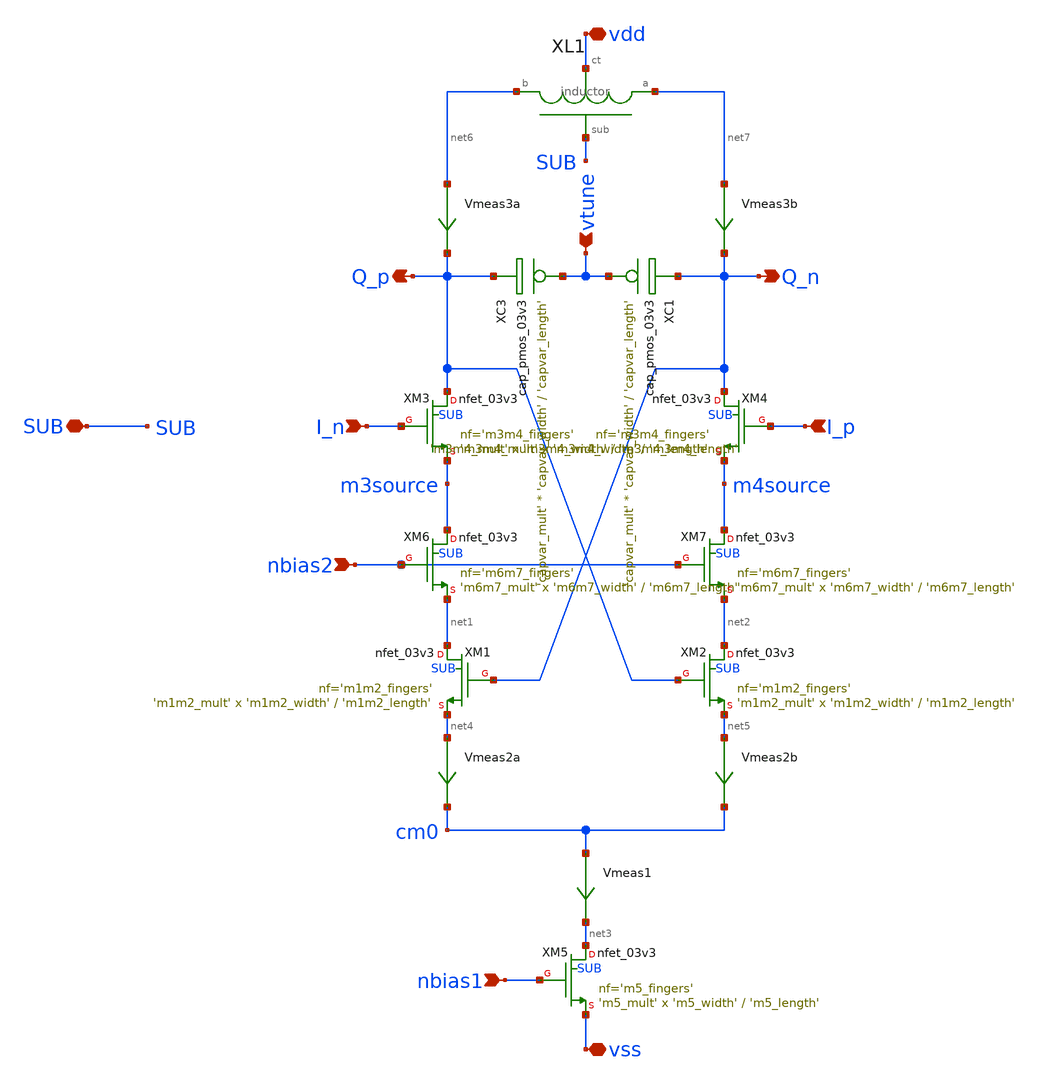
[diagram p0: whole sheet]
** sch_path: sch/vco/half_qvco_cascode_pair.sch
**.subckt half_qvco_cascode_pair SUB vdd vss I_n nbias1 Q_p Q_n I_p vtune nbias2
*.iopin SUB
*.iopin vdd
*.iopin vss
*.ipin I_n
*.ipin nbias1
*.opin Q_p
*.opin Q_n
*.ipin I_p
*.ipin vtune
*.ipin nbias2
XL1 vdd net7 SUB net6 inductor
XM5 net3 nbias1 vss SUB nfet_03v3 L='m5_length' W='m5_width' nf='m5_fingers' ad='int((nf+1)/2) * W/nf * 0.18u'
+ as='int((nf+2)/2) * W/nf * 0.18u' pd='2*int((nf+1)/2) * (W/nf + 0.18u)' ps='2*int((nf+2)/2) * (W/nf + 0.18u)'
+ nrd='0.18u / W' nrs='0.18u / W' sa=0 sb=0 sd=0 m='m5_mult' par='m5_mult'
Vmeas1 cm0 net3 0
.save i(vmeas1)
Vmeas2a net4 cm0 0
.save i(vmeas2a)
Vmeas2b net5 cm0 0
.save i(vmeas2b)
Vmeas3a net6 Q_p 0
.save i(vmeas3a)
Vmeas3b net7 Q_n 0
.save i(vmeas3b)
XM1 net1 Q_n net4 SUB nfet_03v3 L='m1m2_length' W='m1m2_width' nf='m1m2_fingers' ad='int((nf+1)/2) * W/nf * 0.18u'
+ as='int((nf+2)/2) * W/nf * 0.18u' pd='2*int((nf+1)/2) * (W/nf + 0.18u)' ps='2*int((nf+2)/2) * (W/nf + 0.18u)'
+ nrd='0.18u / W' nrs='0.18u / W' sa=0 sb=0 sd=0 m='m1m2_mult' par='m1m2_mult'
XM2 net2 Q_p net5 SUB nfet_03v3 L='m1m2_length' W='m1m2_width' nf='m1m2_fingers' ad='int((nf+1)/2) * W/nf * 0.18u'
+ as='int((nf+2)/2) * W/nf * 0.18u' pd='2*int((nf+1)/2) * (W/nf + 0.18u)' ps='2*int((nf+2)/2) * (W/nf + 0.18u)'
+ nrd='0.18u / W' nrs='0.18u / W' sa=0 sb=0 sd=0 m='m1m2_mult' par='m1m2_mult'
XM3 Q_p I_n m3source SUB nfet_03v3 L='m3m4_length' W='m3m4_width' nf='m3m4_fingers' ad='int((nf+1)/2) * W/nf * 0.18u'
+ as='int((nf+2)/2) * W/nf * 0.18u' pd='2*int((nf+1)/2) * (W/nf + 0.18u)' ps='2*int((nf+2)/2) * (W/nf + 0.18u)'
+ nrd='0.18u / W' nrs='0.18u / W' sa=0 sb=0 sd=0 m='m3m4_mult' par='m3m4_mult'
XM4 Q_n I_p m4source SUB nfet_03v3 L='m3m4_length' W='m3m4_width' nf='m3m4_fingers' ad='int((nf+1)/2) * W/nf * 0.18u'
+ as='int((nf+2)/2) * W/nf * 0.18u' pd='2*int((nf+1)/2) * (W/nf + 0.18u)' ps='2*int((nf+2)/2) * (W/nf + 0.18u)'
+ nrd='0.18u / W' nrs='0.18u / W' sa=0 sb=0 sd=0 m='m3m4_mult' par='m3m4_mult'
XC1 vtune Q_n cap_pmos_03v3 c_width='capvar_width' c_length='capvar_length' m='capvar_mult'
XC3 vtune Q_p cap_pmos_03v3 c_width='capvar_width' c_length='capvar_length' m='capvar_mult'
XM6 m3source nbias2 net1 SUB nfet_03v3 L='m6m7_length' W='m6m7_width' nf='m6m7_fingers' ad='int((nf+1)/2) * W/nf * 0.18u'
+ as='int((nf+2)/2) * W/nf * 0.18u' pd='2*int((nf+1)/2) * (W/nf + 0.18u)' ps='2*int((nf+2)/2) * (W/nf + 0.18u)'
+ nrd='0.18u / W' nrs='0.18u / W' sa=0 sb=0 sd=0 m='m6m7_mult' par='m6m7_mult'
XM7 m4source nbias2 net2 SUB nfet_03v3 L='m6m7_length' W='m6m7_width' nf='m6m7_fingers' ad='int((nf+1)/2) * W/nf * 0.18u'
+ as='int((nf+2)/2) * W/nf * 0.18u' pd='2*int((nf+1)/2) * (W/nf + 0.18u)' ps='2*int((nf+2)/2) * (W/nf + 0.18u)'
+ nrd='0.18u / W' nrs='0.18u / W' sa=0 sb=0 sd=0 m='m6m7_mult' par='m6m7_mult'
**.ends
.end
